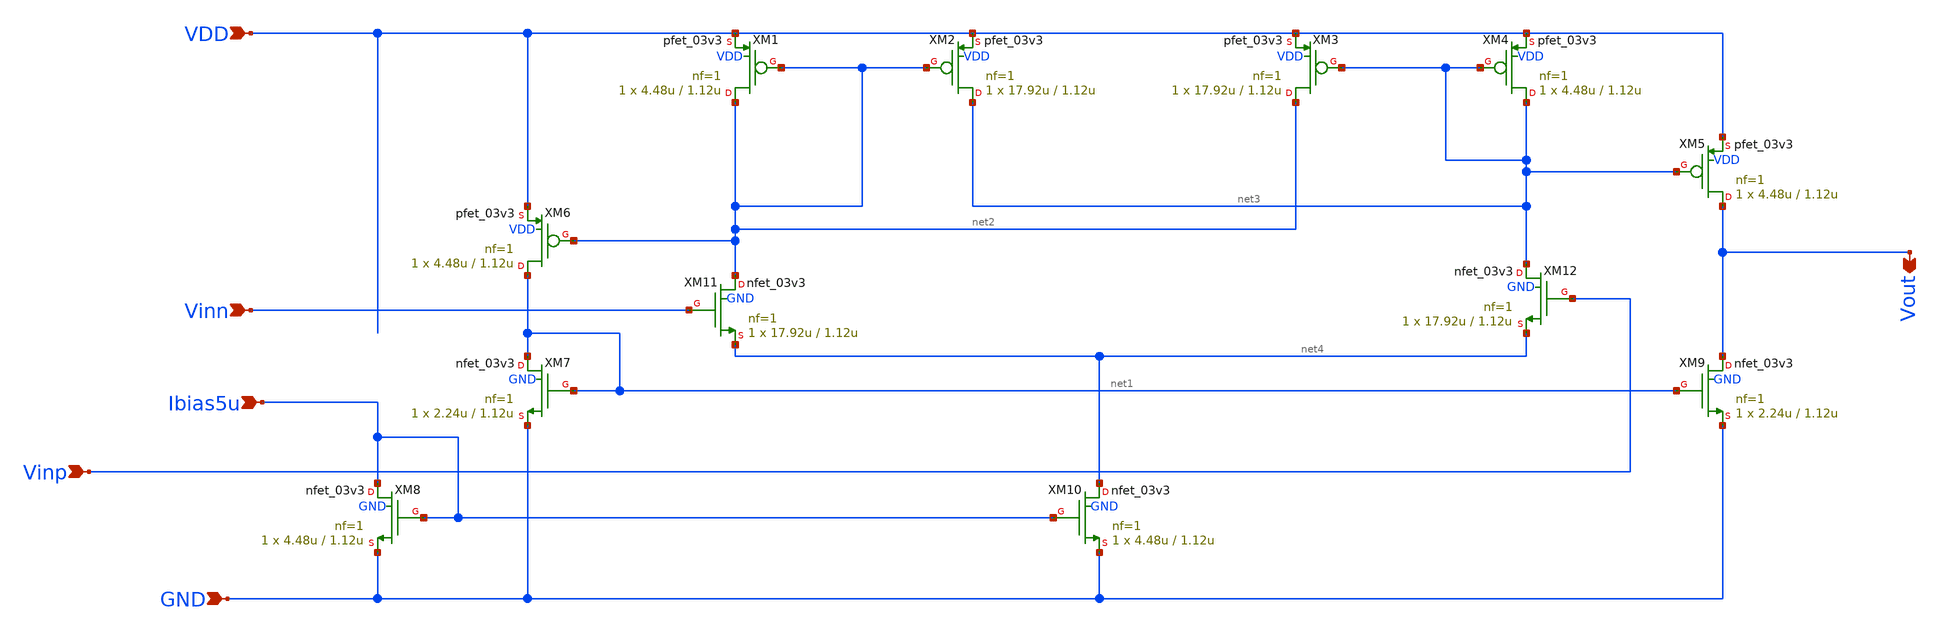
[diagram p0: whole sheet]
** sch_path: comparator/schematic-design/coc_forsym.sch
**.subckt coc_forsym Vout Vinn Vinp VDD GND Ibias5u
*.opin Vout
*.ipin Vinn
*.ipin Vinp
*.ipin VDD
*.ipin GND
*.ipin Ibias5u
XM1 net2 net2 VDD VDD pfet_03v3 L=1.12u W=4.48u nf=1 ad='int((nf+1)/2) * W/nf * 0.18u' as='int((nf+2)/2) * W/nf * 0.18u'
+ pd='2*int((nf+1)/2) * (W/nf + 0.18u)' ps='2*int((nf+2)/2) * (W/nf + 0.18u)' nrd='0.18u / W' nrs='0.18u / W'
+ sa=0 sb=0 sd=0 m=1 par=1
XM2 net3 net2 VDD VDD pfet_03v3 L=1.12u W=17.92u nf=1 ad='int((nf+1)/2) * W/nf * 0.18u' as='int((nf+2)/2) * W/nf * 0.18u'
+ pd='2*int((nf+1)/2) * (W/nf + 0.18u)' ps='2*int((nf+2)/2) * (W/nf + 0.18u)' nrd='0.18u / W' nrs='0.18u / W'
+ sa=0 sb=0 sd=0 m=1 par=1
XM3 net2 net3 VDD VDD pfet_03v3 L=1.12u W=17.92u nf=1 ad='int((nf+1)/2) * W/nf * 0.18u' as='int((nf+2)/2) * W/nf * 0.18u'
+ pd='2*int((nf+1)/2) * (W/nf + 0.18u)' ps='2*int((nf+2)/2) * (W/nf + 0.18u)' nrd='0.18u / W' nrs='0.18u / W'
+ sa=0 sb=0 sd=0 m=1 par=1
XM4 net3 net3 VDD VDD pfet_03v3 L=1.12u W=4.48u nf=1 ad='int((nf+1)/2) * W/nf * 0.18u' as='int((nf+2)/2) * W/nf * 0.18u'
+ pd='2*int((nf+1)/2) * (W/nf + 0.18u)' ps='2*int((nf+2)/2) * (W/nf + 0.18u)' nrd='0.18u / W' nrs='0.18u / W'
+ sa=0 sb=0 sd=0 m=1 par=1
XM5 Vout net3 VDD VDD pfet_03v3 L=1.12u W=4.48u nf=1 ad='int((nf+1)/2) * W/nf * 0.18u' as='int((nf+2)/2) * W/nf * 0.18u'
+ pd='2*int((nf+1)/2) * (W/nf + 0.18u)' ps='2*int((nf+2)/2) * (W/nf + 0.18u)' nrd='0.18u / W' nrs='0.18u / W'
+ sa=0 sb=0 sd=0 m=1 par=1
XM6 net1 net2 VDD VDD pfet_03v3 L=1.12u W=4.48u nf=1 ad='int((nf+1)/2) * W/nf * 0.18u' as='int((nf+2)/2) * W/nf * 0.18u'
+ pd='2*int((nf+1)/2) * (W/nf + 0.18u)' ps='2*int((nf+2)/2) * (W/nf + 0.18u)' nrd='0.18u / W' nrs='0.18u / W'
+ sa=0 sb=0 sd=0 m=1 par=1
XM7 net1 net1 GND GND nfet_03v3 L=1.12u W=2.24u nf=1 ad='int((nf+1)/2) * W/nf * 0.18u' as='int((nf+2)/2) * W/nf * 0.18u'
+ pd='2*int((nf+1)/2) * (W/nf + 0.18u)' ps='2*int((nf+2)/2) * (W/nf + 0.18u)' nrd='0.18u / W' nrs='0.18u / W'
+ sa=0 sb=0 sd=0 m=1 par=1
XM8 Ibias5u Ibias5u GND GND nfet_03v3 L=1.12u W=4.48u nf=1 ad='int((nf+1)/2) * W/nf * 0.18u' as='int((nf+2)/2) * W/nf * 0.18u'
+ pd='2*int((nf+1)/2) * (W/nf + 0.18u)' ps='2*int((nf+2)/2) * (W/nf + 0.18u)' nrd='0.18u / W' nrs='0.18u / W'
+ sa=0 sb=0 sd=0 m=1 par=1
XM9 Vout net1 GND GND nfet_03v3 L=1.12u W=2.24u nf=1 ad='int((nf+1)/2) * W/nf * 0.18u' as='int((nf+2)/2) * W/nf * 0.18u'
+ pd='2*int((nf+1)/2) * (W/nf + 0.18u)' ps='2*int((nf+2)/2) * (W/nf + 0.18u)' nrd='0.18u / W' nrs='0.18u / W'
+ sa=0 sb=0 sd=0 m=1 par=1
XM10 net4 Ibias5u GND GND nfet_03v3 L=1.12u W=4.48u nf=1 ad='int((nf+1)/2) * W/nf * 0.18u' as='int((nf+2)/2) * W/nf * 0.18u'
+ pd='2*int((nf+1)/2) * (W/nf + 0.18u)' ps='2*int((nf+2)/2) * (W/nf + 0.18u)' nrd='0.18u / W' nrs='0.18u / W'
+ sa=0 sb=0 sd=0 m=1 par=1
XM11 net2 Vinn net4 GND nfet_03v3 L=1.12u W=17.92u nf=1 ad='int((nf+1)/2) * W/nf * 0.18u' as='int((nf+2)/2) * W/nf * 0.18u'
+ pd='2*int((nf+1)/2) * (W/nf + 0.18u)' ps='2*int((nf+2)/2) * (W/nf + 0.18u)' nrd='0.18u / W' nrs='0.18u / W'
+ sa=0 sb=0 sd=0 m=1 par=1
XM12 net3 Vinp net4 GND nfet_03v3 L=1.12u W=17.92u nf=1 ad='int((nf+1)/2) * W/nf * 0.18u' as='int((nf+2)/2) * W/nf * 0.18u'
+ pd='2*int((nf+1)/2) * (W/nf + 0.18u)' ps='2*int((nf+2)/2) * (W/nf + 0.18u)' nrd='0.18u / W' nrs='0.18u / W'
+ sa=0 sb=0 sd=0 m=1 par=1
**.ends
.end
